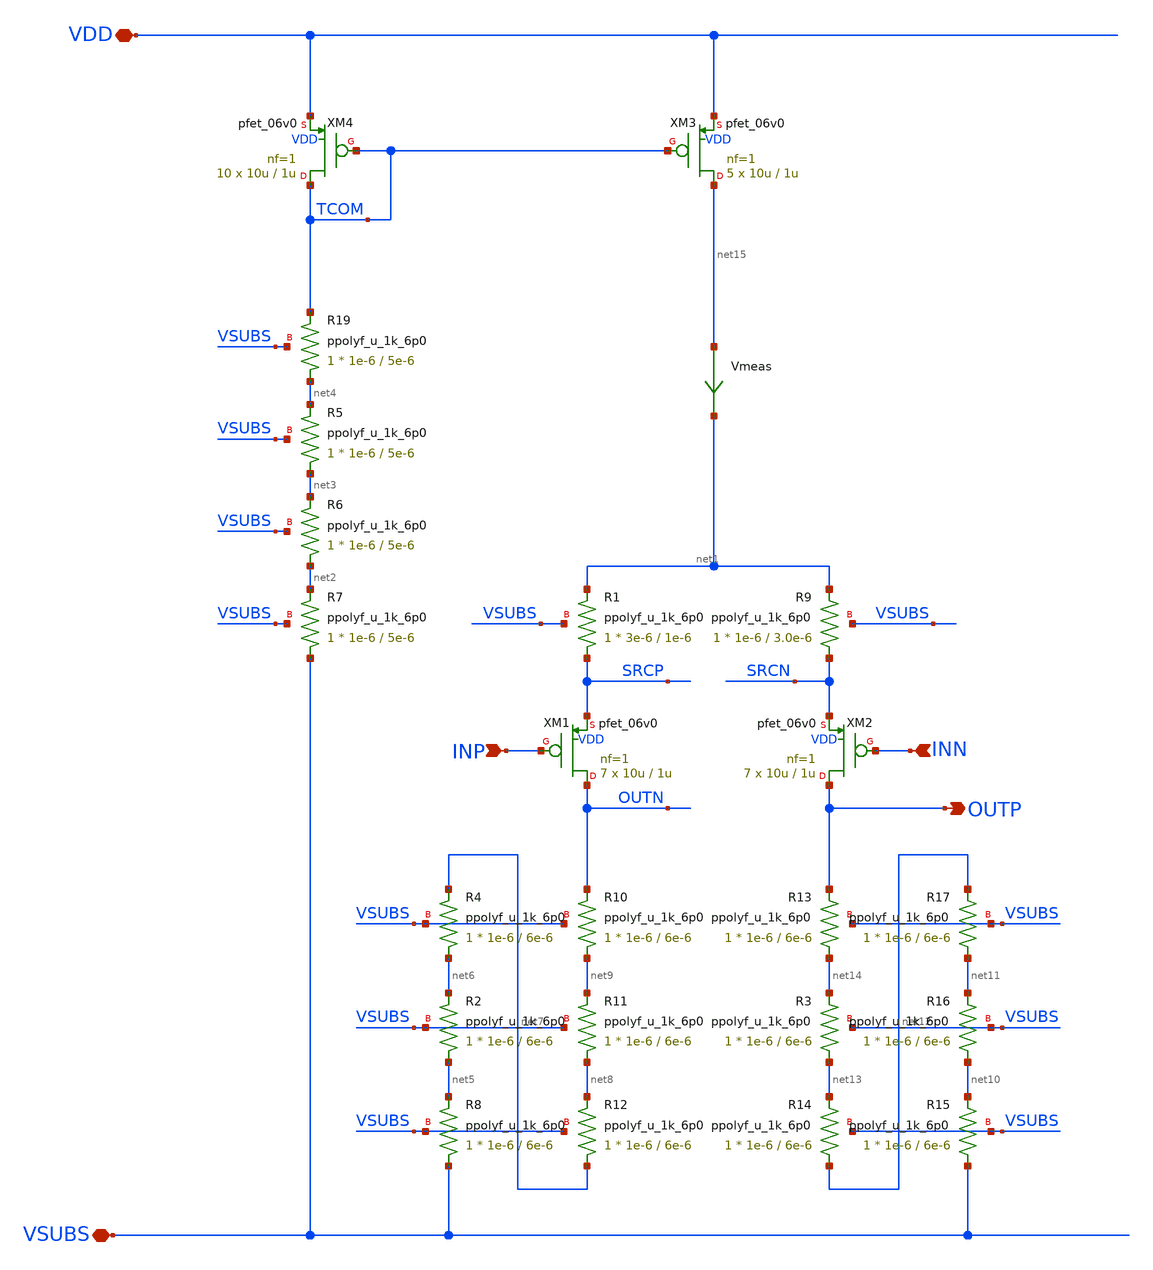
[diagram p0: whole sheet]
** sch_path: xschem/ip_amplifier.sch
**.subckt ip_amplifier VDD VSUBS INP INN OUTP
*.iopin VDD
*.iopin VSUBS
*.ipin INP
*.ipin INN
*.opin OUTP
XM4 TCOM TCOM VDD VDD pfet_06v0 L=1u W=10u nf=1 ad='int((nf+1)/2) * W/nf * 0.18u' as='int((nf+2)/2) * W/nf * 0.18u'
+ pd='2*int((nf+1)/2) * (W/nf + 0.18u)' ps='2*int((nf+2)/2) * (W/nf + 0.18u)' nrd='0.18u / W' nrs='0.18u / W'
+ sa=0 sb=0 sd=0 m=10 par=10
XM3 net15 TCOM VDD VDD pfet_06v0 L=1u W=10u nf=1 ad='int((nf+1)/2) * W/nf * 0.18u' as='int((nf+2)/2) * W/nf * 0.18u'
+ pd='2*int((nf+1)/2) * (W/nf + 0.18u)' ps='2*int((nf+2)/2) * (W/nf + 0.18u)' nrd='0.18u / W' nrs='0.18u / W'
+ sa=0 sb=0 sd=0 m=5 par=5
XM1 OUTN INP SRCP VDD pfet_06v0 L=1u W=10u nf=1 ad='int((nf+1)/2) * W/nf * 0.18u' as='int((nf+2)/2) * W/nf * 0.18u'
+ pd='2*int((nf+1)/2) * (W/nf + 0.18u)' ps='2*int((nf+2)/2) * (W/nf + 0.18u)' nrd='0.18u / W' nrs='0.18u / W'
+ sa=0 sb=0 sd=0 m=7 par=7
XM2 OUTP INN SRCN VDD pfet_06v0 L=1u W=10u nf=1 ad='int((nf+1)/2) * W/nf * 0.18u' as='int((nf+2)/2) * W/nf * 0.18u'
+ pd='2*int((nf+1)/2) * (W/nf + 0.18u)' ps='2*int((nf+2)/2) * (W/nf + 0.18u)' nrd='0.18u / W' nrs='0.18u / W'
+ sa=0 sb=0 sd=0 m=7 par=7
XR19 net4 TCOM VSUBS ppolyf_u_1k_6p0 r_width=1e-6 r_length=5e-6 m=1
XR5 net3 net4 VSUBS ppolyf_u_1k_6p0 r_width=1e-6 r_length=5e-6 m=1
XR4 net6 net7 VSUBS ppolyf_u_1k_6p0 r_width=1e-6 r_length=6e-6 m=1
XR2 net5 net6 VSUBS ppolyf_u_1k_6p0 r_width=1e-6 r_length=6e-6 m=1
XR8 VSUBS net5 VSUBS ppolyf_u_1k_6p0 r_width=1e-6 r_length=6e-6 m=1
XR12 net7 net8 VSUBS ppolyf_u_1k_6p0 r_width=1e-6 r_length=6e-6 m=1
XR11 net8 net9 VSUBS ppolyf_u_1k_6p0 r_width=1e-6 r_length=6e-6 m=1
XR10 net9 OUTN VSUBS ppolyf_u_1k_6p0 r_width=1e-6 r_length=6e-6 m=1
XR13 net14 OUTP VSUBS ppolyf_u_1k_6p0 r_width=1e-6 r_length=6e-6 m=1
XR3 net13 net14 VSUBS ppolyf_u_1k_6p0 r_width=1e-6 r_length=6e-6 m=1
XR14 net12 net13 VSUBS ppolyf_u_1k_6p0 r_width=1e-6 r_length=6e-6 m=1
XR15 VSUBS net10 VSUBS ppolyf_u_1k_6p0 r_width=1e-6 r_length=6e-6 m=1
XR16 net10 net11 VSUBS ppolyf_u_1k_6p0 r_width=1e-6 r_length=6e-6 m=1
XR17 net11 net12 VSUBS ppolyf_u_1k_6p0 r_width=1e-6 r_length=6e-6 m=1
XR9 SRCN net1 VSUBS ppolyf_u_1k_6p0 r_width=1e-6 r_length=3.0e-6 m=1
XR1 SRCP net1 VSUBS ppolyf_u_1k_6p0 r_width=3e-6 r_length=1e-6 m=1
XR6 net2 net3 VSUBS ppolyf_u_1k_6p0 r_width=1e-6 r_length=5e-6 m=1
XR7 VSUBS net2 VSUBS ppolyf_u_1k_6p0 r_width=1e-6 r_length=5e-6 m=1
Vmeas net15 net1 0
**.ends
.end
